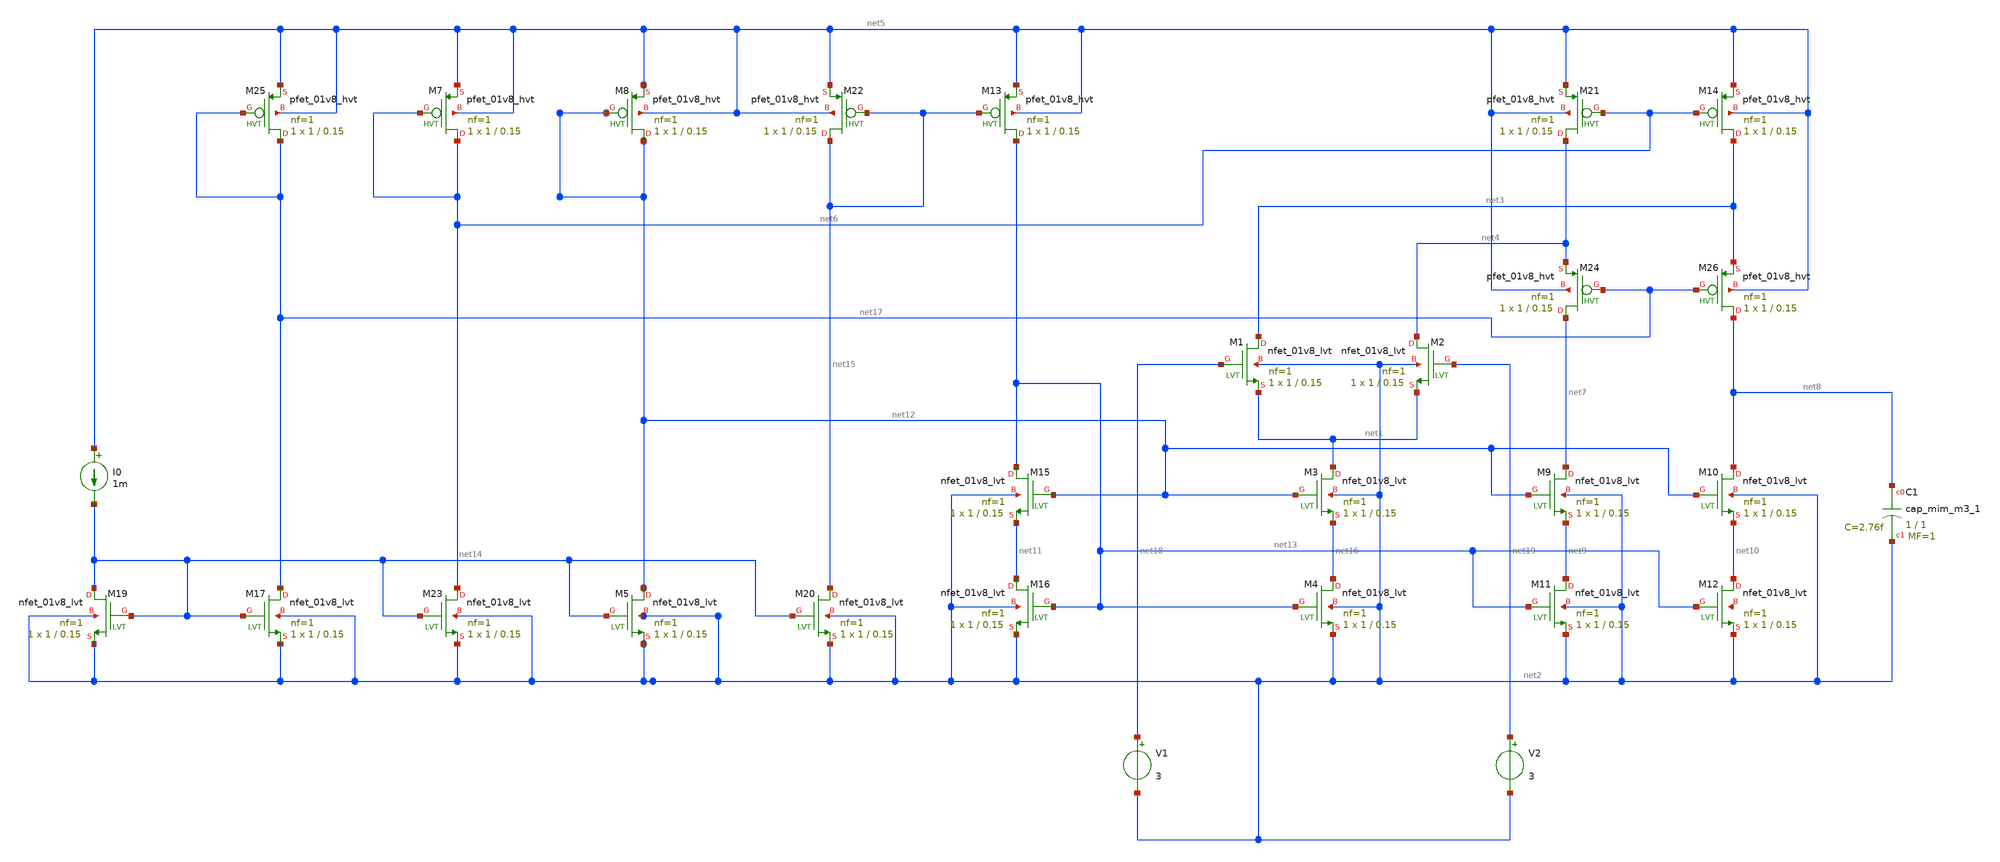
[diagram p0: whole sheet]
** sch_path: xschem/ip_block/opamp/folded_cas_xiaoyi/OTA.sch
**.subckt OTA
XM1 net3 net18 net1 net2 sky130_fd_pr__nfet_01v8_lvt L=0.15 W=1 nf=1 ad='int((nf+1)/2) * W/nf * 0.29'
+ as='int((nf+2)/2) * W/nf * 0.29' pd='2*int((nf+1)/2) * (W/nf + 0.29)' ps='2*int((nf+2)/2) * (W/nf + 0.29)'
+ nrd='0.29 / W' nrs='0.29 / W' sa=0 sb=0 sd=0 mult=1 m=1
XM2 net4 net19 net1 net2 sky130_fd_pr__nfet_01v8_lvt L=0.15 W=1 nf=1 ad='int((nf+1)/2) * W/nf * 0.29'
+ as='int((nf+2)/2) * W/nf * 0.29' pd='2*int((nf+1)/2) * (W/nf + 0.29)' ps='2*int((nf+2)/2) * (W/nf + 0.29)'
+ nrd='0.29 / W' nrs='0.29 / W' sa=0 sb=0 sd=0 mult=1 m=1
XM3 net1 net12 net16 net2 sky130_fd_pr__nfet_01v8_lvt L=0.15 W=1 nf=1 ad='int((nf+1)/2) * W/nf * 0.29'
+ as='int((nf+2)/2) * W/nf * 0.29' pd='2*int((nf+1)/2) * (W/nf + 0.29)' ps='2*int((nf+2)/2) * (W/nf + 0.29)'
+ nrd='0.29 / W' nrs='0.29 / W' sa=0 sb=0 sd=0 mult=1 m=1
XM4 net16 net13 net2 net2 sky130_fd_pr__nfet_01v8_lvt L=0.15 W=1 nf=1 ad='int((nf+1)/2) * W/nf * 0.29'
+ as='int((nf+2)/2) * W/nf * 0.29' pd='2*int((nf+1)/2) * (W/nf + 0.29)' ps='2*int((nf+2)/2) * (W/nf + 0.29)'
+ nrd='0.29 / W' nrs='0.29 / W' sa=0 sb=0 sd=0 mult=1 m=1
XM9 net7 net12 net9 net2 sky130_fd_pr__nfet_01v8_lvt L=0.15 W=1 nf=1 ad='int((nf+1)/2) * W/nf * 0.29'
+ as='int((nf+2)/2) * W/nf * 0.29' pd='2*int((nf+1)/2) * (W/nf + 0.29)' ps='2*int((nf+2)/2) * (W/nf + 0.29)'
+ nrd='0.29 / W' nrs='0.29 / W' sa=0 sb=0 sd=0 mult=1 m=1
XM10 net8 net12 net10 net2 sky130_fd_pr__nfet_01v8_lvt L=0.15 W=1 nf=1 ad='int((nf+1)/2) * W/nf * 0.29'
+ as='int((nf+2)/2) * W/nf * 0.29' pd='2*int((nf+1)/2) * (W/nf + 0.29)' ps='2*int((nf+2)/2) * (W/nf + 0.29)'
+ nrd='0.29 / W' nrs='0.29 / W' sa=0 sb=0 sd=0 mult=1 m=1
XM11 net9 net13 net2 net2 sky130_fd_pr__nfet_01v8_lvt L=0.15 W=1 nf=1 ad='int((nf+1)/2) * W/nf * 0.29'
+ as='int((nf+2)/2) * W/nf * 0.29' pd='2*int((nf+1)/2) * (W/nf + 0.29)' ps='2*int((nf+2)/2) * (W/nf + 0.29)'
+ nrd='0.29 / W' nrs='0.29 / W' sa=0 sb=0 sd=0 mult=1 m=1
XM12 net10 net13 net2 net20 sky130_fd_pr__nfet_01v8_lvt L=0.15 W=1 nf=1 ad='int((nf+1)/2) * W/nf * 0.29'
+ as='int((nf+2)/2) * W/nf * 0.29' pd='2*int((nf+1)/2) * (W/nf + 0.29)' ps='2*int((nf+2)/2) * (W/nf + 0.29)'
+ nrd='0.29 / W' nrs='0.29 / W' sa=0 sb=0 sd=0 mult=1 m=1
XM15 net13 net12 net11 net2 sky130_fd_pr__nfet_01v8_lvt L=0.15 W=1 nf=1 ad='int((nf+1)/2) * W/nf * 0.29'
+ as='int((nf+2)/2) * W/nf * 0.29' pd='2*int((nf+1)/2) * (W/nf + 0.29)' ps='2*int((nf+2)/2) * (W/nf + 0.29)'
+ nrd='0.29 / W' nrs='0.29 / W' sa=0 sb=0 sd=0 mult=1 m=1
XM16 net11 net13 net2 net2 sky130_fd_pr__nfet_01v8_lvt L=0.15 W=1 nf=1 ad='int((nf+1)/2) * W/nf * 0.29'
+ as='int((nf+2)/2) * W/nf * 0.29' pd='2*int((nf+1)/2) * (W/nf + 0.29)' ps='2*int((nf+2)/2) * (W/nf + 0.29)'
+ nrd='0.29 / W' nrs='0.29 / W' sa=0 sb=0 sd=0 mult=1 m=1
XM19 net14 net14 net2 net2 sky130_fd_pr__nfet_01v8_lvt L=0.15 W=1 nf=1 ad='int((nf+1)/2) * W/nf * 0.29'
+ as='int((nf+2)/2) * W/nf * 0.29' pd='2*int((nf+1)/2) * (W/nf + 0.29)' ps='2*int((nf+2)/2) * (W/nf + 0.29)'
+ nrd='0.29 / W' nrs='0.29 / W' sa=0 sb=0 sd=0 mult=1 m=1
XM20 net15 net14 net2 net2 sky130_fd_pr__nfet_01v8_lvt L=0.15 W=1 nf=1 ad='int((nf+1)/2) * W/nf * 0.29'
+ as='int((nf+2)/2) * W/nf * 0.29' pd='2*int((nf+1)/2) * (W/nf + 0.29)' ps='2*int((nf+2)/2) * (W/nf + 0.29)'
+ nrd='0.29 / W' nrs='0.29 / W' sa=0 sb=0 sd=0 mult=1 m=1
XM17 net17 net14 net2 net2 sky130_fd_pr__nfet_01v8_lvt L=0.15 W=1 nf=1 ad='int((nf+1)/2) * W/nf * 0.29'
+ as='int((nf+2)/2) * W/nf * 0.29' pd='2*int((nf+1)/2) * (W/nf + 0.29)' ps='2*int((nf+2)/2) * (W/nf + 0.29)'
+ nrd='0.29 / W' nrs='0.29 / W' sa=0 sb=0 sd=0 mult=1 m=1
XM23 net6 net14 net2 net2 sky130_fd_pr__nfet_01v8_lvt L=0.15 W=1 nf=1 ad='int((nf+1)/2) * W/nf * 0.29'
+ as='int((nf+2)/2) * W/nf * 0.29' pd='2*int((nf+1)/2) * (W/nf + 0.29)' ps='2*int((nf+2)/2) * (W/nf + 0.29)'
+ nrd='0.29 / W' nrs='0.29 / W' sa=0 sb=0 sd=0 mult=1 m=1
XM25 net17 net17 net5 net5 sky130_fd_pr__pfet_01v8_hvt L=0.15 W=1 nf=1 ad='int((nf+1)/2) * W/nf * 0.29'
+ as='int((nf+2)/2) * W/nf * 0.29' pd='2*int((nf+1)/2) * (W/nf + 0.29)' ps='2*int((nf+2)/2) * (W/nf + 0.29)'
+ nrd='0.29 / W' nrs='0.29 / W' sa=0 sb=0 sd=0 mult=1 m=1
XM5 net12 net14 net2 net2 sky130_fd_pr__nfet_01v8_lvt L=0.15 W=1 nf=1 ad='int((nf+1)/2) * W/nf * 0.29'
+ as='int((nf+2)/2) * W/nf * 0.29' pd='2*int((nf+1)/2) * (W/nf + 0.29)' ps='2*int((nf+2)/2) * (W/nf + 0.29)'
+ nrd='0.29 / W' nrs='0.29 / W' sa=0 sb=0 sd=0 mult=1 m=1
XM7 net6 net6 net5 net5 sky130_fd_pr__pfet_01v8_hvt L=0.15 W=1 nf=1 ad='int((nf+1)/2) * W/nf * 0.29'
+ as='int((nf+2)/2) * W/nf * 0.29' pd='2*int((nf+1)/2) * (W/nf + 0.29)' ps='2*int((nf+2)/2) * (W/nf + 0.29)'
+ nrd='0.29 / W' nrs='0.29 / W' sa=0 sb=0 sd=0 mult=1 m=1
XM8 net12 net12 net5 net5 sky130_fd_pr__pfet_01v8_hvt L=0.15 W=1 nf=1 ad='int((nf+1)/2) * W/nf * 0.29'
+ as='int((nf+2)/2) * W/nf * 0.29' pd='2*int((nf+1)/2) * (W/nf + 0.29)' ps='2*int((nf+2)/2) * (W/nf + 0.29)'
+ nrd='0.29 / W' nrs='0.29 / W' sa=0 sb=0 sd=0 mult=1 m=1
XM13 net13 net15 net5 net5 sky130_fd_pr__pfet_01v8_hvt L=0.15 W=1 nf=1 ad='int((nf+1)/2) * W/nf * 0.29'
+ as='int((nf+2)/2) * W/nf * 0.29' pd='2*int((nf+1)/2) * (W/nf + 0.29)' ps='2*int((nf+2)/2) * (W/nf + 0.29)'
+ nrd='0.29 / W' nrs='0.29 / W' sa=0 sb=0 sd=0 mult=1 m=1
XM14 net3 net6 net5 net5 sky130_fd_pr__pfet_01v8_hvt L=0.15 W=1 nf=1 ad='int((nf+1)/2) * W/nf * 0.29'
+ as='int((nf+2)/2) * W/nf * 0.29' pd='2*int((nf+1)/2) * (W/nf + 0.29)' ps='2*int((nf+2)/2) * (W/nf + 0.29)'
+ nrd='0.29 / W' nrs='0.29 / W' sa=0 sb=0 sd=0 mult=1 m=1
XM21 net4 net6 net5 net5 sky130_fd_pr__pfet_01v8_hvt L=0.15 W=1 nf=1 ad='int((nf+1)/2) * W/nf * 0.29'
+ as='int((nf+2)/2) * W/nf * 0.29' pd='2*int((nf+1)/2) * (W/nf + 0.29)' ps='2*int((nf+2)/2) * (W/nf + 0.29)'
+ nrd='0.29 / W' nrs='0.29 / W' sa=0 sb=0 sd=0 mult=1 m=1
XM22 net15 net15 net5 net5 sky130_fd_pr__pfet_01v8_hvt L=0.15 W=1 nf=1 ad='int((nf+1)/2) * W/nf * 0.29'
+ as='int((nf+2)/2) * W/nf * 0.29' pd='2*int((nf+1)/2) * (W/nf + 0.29)' ps='2*int((nf+2)/2) * (W/nf + 0.29)'
+ nrd='0.29 / W' nrs='0.29 / W' sa=0 sb=0 sd=0 mult=1 m=1
XM24 net7 net17 net4 net5 sky130_fd_pr__pfet_01v8_hvt L=0.15 W=1 nf=1 ad='int((nf+1)/2) * W/nf * 0.29'
+ as='int((nf+2)/2) * W/nf * 0.29' pd='2*int((nf+1)/2) * (W/nf + 0.29)' ps='2*int((nf+2)/2) * (W/nf + 0.29)'
+ nrd='0.29 / W' nrs='0.29 / W' sa=0 sb=0 sd=0 mult=1 m=1
XM26 net8 net17 net3 net5 sky130_fd_pr__pfet_01v8_hvt L=0.15 W=1 nf=1 ad='int((nf+1)/2) * W/nf * 0.29'
+ as='int((nf+2)/2) * W/nf * 0.29' pd='2*int((nf+1)/2) * (W/nf + 0.29)' ps='2*int((nf+2)/2) * (W/nf + 0.29)'
+ nrd='0.29 / W' nrs='0.29 / W' sa=0 sb=0 sd=0 mult=1 m=1
I0 net5 net14 1m
V1 net18 net2 3
V2 net19 net2 3
XC1 net8 net2 sky130_fd_pr__cap_mim_m3_1 W=1 L=1 MF=1 m=1
**.ends
.end
